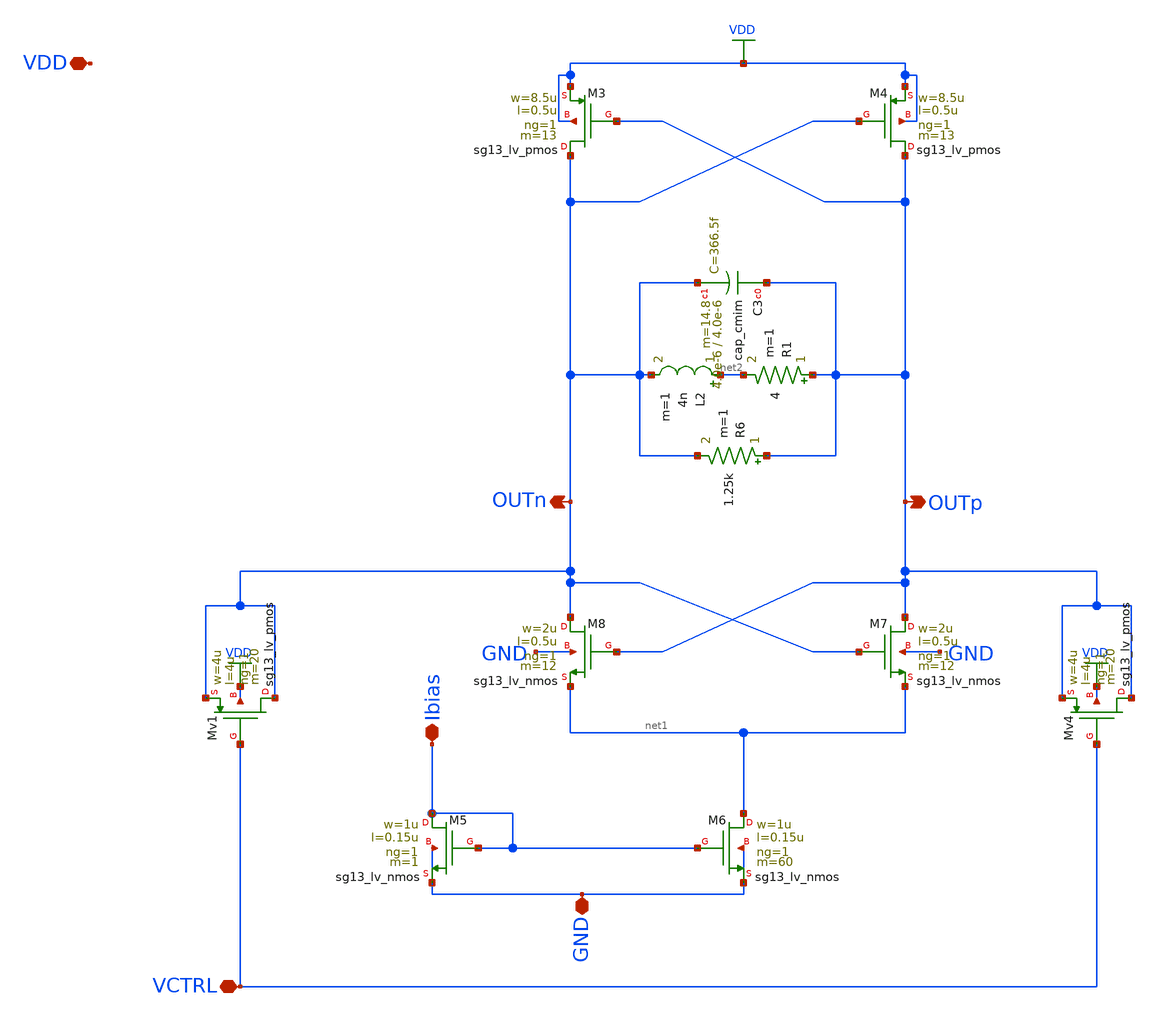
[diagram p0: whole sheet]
** sch_path: schematic/blocks/lc-vco/LC_VCO.sch
**.subckt LC_VCO VDD OUTp OUTn GND VCTRL Ibias
*.iopin VDD
*.opin OUTp
*.opin OUTn
*.iopin GND
*.iopin VCTRL
*.iopin Ibias
L2 net2 OUTn 4n m=1
XM6 net1 Ibias GND GND sg13_lv_nmos w=1u l=0.15u ng=1 m=60 mm_ok=1
XM5 Ibias Ibias GND GND sg13_lv_nmos w=1u l=0.15u ng=1 m=1 mm_ok=1
XM4 OUTp OUTn VDD VDD sg13_lv_pmos w=8.5u l=0.5u ng=1 m=13 mm_ok=1
X5M3 OUTn OUTp VDD VDD sg13_lv_pmos w=8.5u l=0.5u ng=1 m=13 mm_ok=1
XM7 OUTp OUTn net1 GND sg13_lv_nmos w=2u l=0.5u ng=1 m=12 mm_ok=1
XM8 OUTn OUTp net1 GND sg13_lv_nmos w=2u l=0.5u ng=1 m=12 mm_ok=1
R6 OUTp OUTn 1.25k m=1
R1 OUTp net2 4 m=1
XC3 OUTp OUTn cap_cmim w=4.0e-6 l=4.0e-6 m=14.8 mm_ok=1
XMv4 OUTp VCTRL OUTp VDD sg13_lv_pmos w=4u l=4u ng=1 m=20 mm_ok=1
XMv1 OUTn VCTRL OUTn VDD sg13_lv_pmos w=4u l=4u ng=1 m=20 mm_ok=1
**.ends
.GLOBAL VDD
.end
